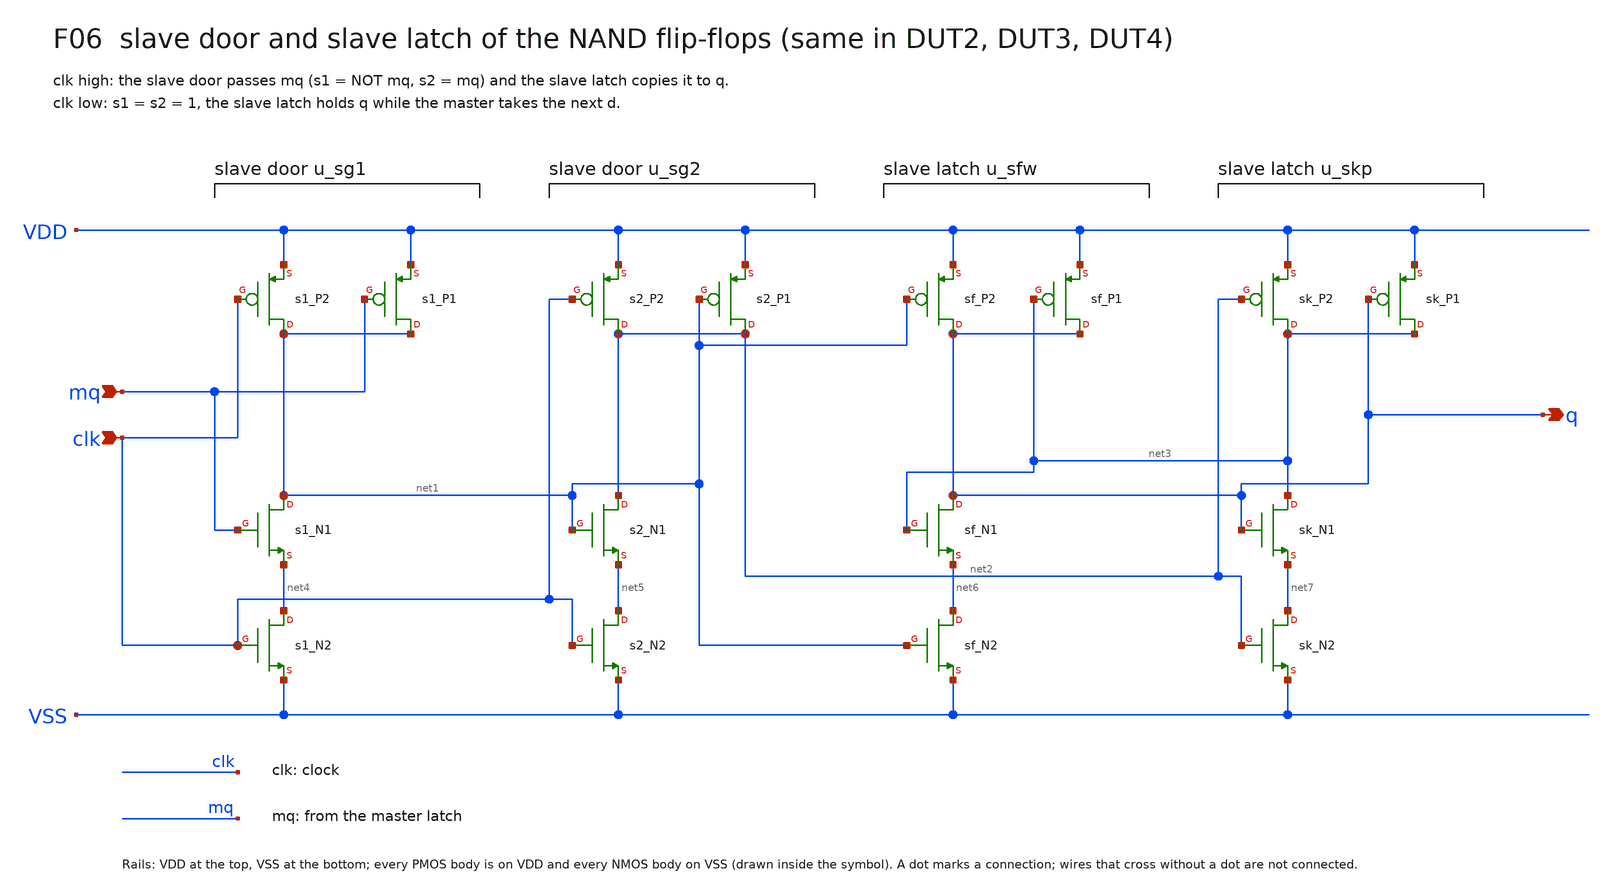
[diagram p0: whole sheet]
** sch_path: xschem/focus/F06_slave.sch
**.subckt F06_slave mq clk q
*.ipin mq
*.ipin clk
*.opin q
Xs1_N2 net4 clk VSS VSS nfet_05v0 L=0.6u W=0.82u nf=1 m=1
Xs1_N1 net1 mq net4 VSS nfet_05v0 L=0.6u W=0.82u nf=1 m=1
Xs1_P2 net1 clk VDD VDD pfet_05v0 L=0.5u W=1.13u nf=1 m=1
Xs1_P1 net1 mq VDD VDD pfet_05v0 L=0.5u W=1.13u nf=1 m=1
Xs2_N2 net5 clk VSS VSS nfet_05v0 L=0.6u W=0.82u nf=1 m=1
Xs2_N1 net2 net1 net5 VSS nfet_05v0 L=0.6u W=0.82u nf=1 m=1
Xs2_P2 net2 clk VDD VDD pfet_05v0 L=0.5u W=1.13u nf=1 m=1
Xs2_P1 net2 net1 VDD VDD pfet_05v0 L=0.5u W=1.13u nf=1 m=1
Xsf_N2 net6 net1 VSS VSS nfet_05v0 L=0.6u W=0.82u nf=1 m=1
Xsf_N1 q net3 net6 VSS nfet_05v0 L=0.6u W=0.82u nf=1 m=1
Xsf_P2 q net1 VDD VDD pfet_05v0 L=0.5u W=1.13u nf=1 m=1
Xsf_P1 q net3 VDD VDD pfet_05v0 L=0.5u W=1.13u nf=1 m=1
Xsk_N2 net7 net2 VSS VSS nfet_05v0 L=0.6u W=0.82u nf=1 m=1
Xsk_N1 net3 q net7 VSS nfet_05v0 L=0.6u W=0.82u nf=1 m=1
Xsk_P2 net3 net2 VDD VDD pfet_05v0 L=0.5u W=1.13u nf=1 m=1
Xsk_P1 net3 q VDD VDD pfet_05v0 L=0.5u W=1.13u nf=1 m=1
**.ends
.end
